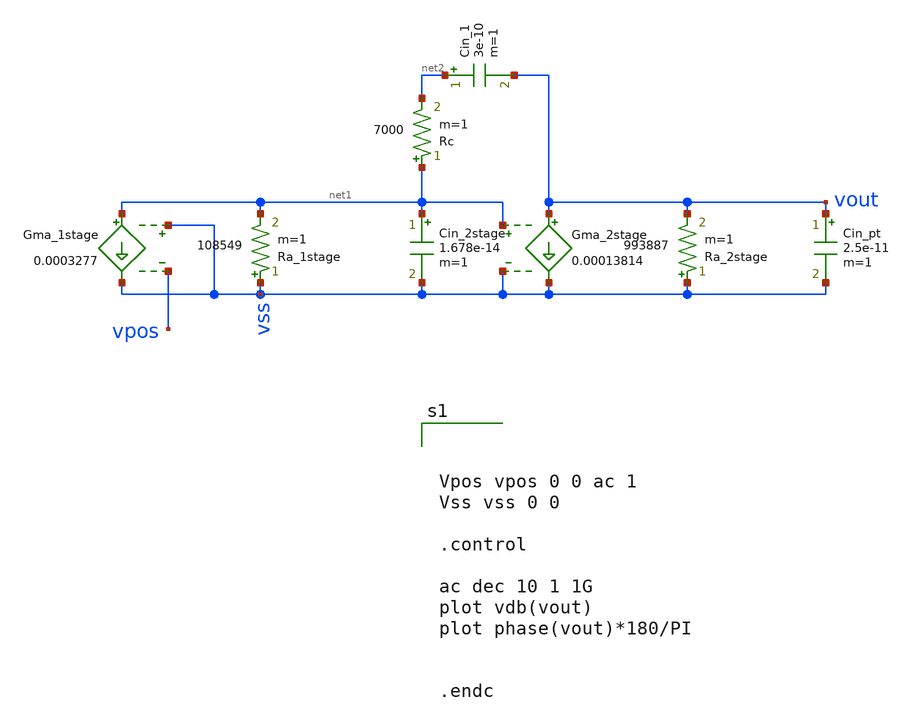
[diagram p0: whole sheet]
** sch_path: test-python/Tesis_notebooks/xschem/OpAmp_2stage_ss_tb.sch
**.subckt OpAmp_2stage_ss_tb
Gma_1stage net1 vss vss vpos 0.0003277
Ra_1stage vss net1 108549 m=1
Cin_pt vout vss 2.5e-11 m=1
Cin_2stage net1 vss 1.678e-14 m=1
Gma_2stage vout vss net1 vss 0.00013814
Ra_2stage vss vout 993887 m=1
Cin_1 net2 vout 3e-10 m=1
Rc net1 net2 7000 m=1
**** begin user architecture code



Vpos vpos 0 0 ac 1
Vss vss 0 0

.control

ac dec 10 1 1G
plot vdb(vout)
plot phase(vout)*180/PI


.endc



**** end user architecture code
**.ends
.end
